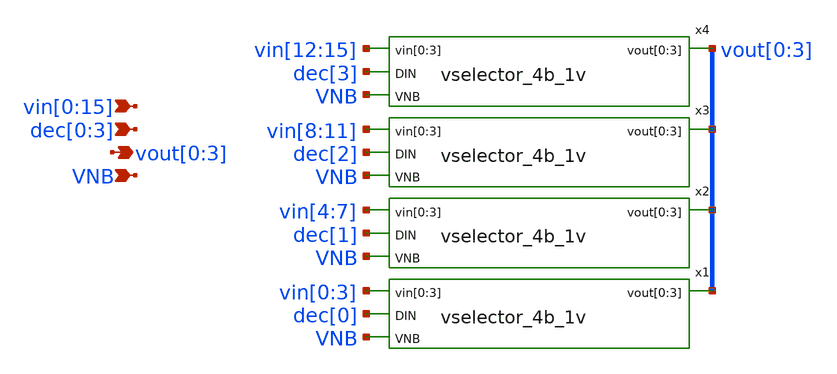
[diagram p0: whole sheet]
** sch_path: xschem/vselector_6b_1v_stage_2.sch
**.subckt vselector_6b_1v_stage_2
*+ vin[0],vin[1],vin[2],vin[3],vin[4],vin[5],vin[6],vin[7],vin[8],vin[9],vin[10],vin[11],vin[12],vin[13],vin[14],vin[15] vout[0],vout[1],vout[2],vout[3] VNB dec[0],dec[1],dec[2],dec[3]
*.ipin
*+ vin[0],vin[1],vin[2],vin[3],vin[4],vin[5],vin[6],vin[7],vin[8],vin[9],vin[10],vin[11],vin[12],vin[13],vin[14],vin[15]
*.opin vout[0],vout[1],vout[2],vout[3]
*.ipin VNB
*.ipin dec[0],dec[1],dec[2],dec[3]
x1 vin[0] vin[1] vin[2] vin[3] dec[0] vout[0] vout[1] vout[2] vout[3] VNB vselector_4b_1v
x2 vin[4] vin[5] vin[6] vin[7] dec[1] vout[0] vout[1] vout[2] vout[3] VNB vselector_4b_1v
x3 vin[8] vin[9] vin[10] vin[11] dec[2] vout[0] vout[1] vout[2] vout[3] VNB vselector_4b_1v
x4 vin[12] vin[13] vin[14] vin[15] dec[3] vout[0] vout[1] vout[2] vout[3] VNB vselector_4b_1v
**.ends

* expanding   symbol:  vselector_4b_1v.sym # of pins=4
** sym_path: xschem/vselector_4b_1v.sym
** sch_path: xschem/vselector_4b_1v.sch
.subckt vselector_4b_1v vin[0] vin[1] vin[2] vin[3] DIN vout[0] vout[1] vout[2] vout[3] VNB
*.ipin vin[0],vin[1],vin[2],vin[3]
*.opin vout[0],vout[1],vout[2],vout[3]
*.ipin VNB
*.ipin DIN
.param wp=0.42 wn=0.42 l=0.5

XM1 vout[0] DIN vin[0] VNB sky130_fd_pr__nfet_g5v0d10v5 L=l W=wn nf=1 ad='int((nf+1)/2) * W/nf * 0.29'
+ as='int((nf+2)/2) * W/nf * 0.29' pd='2*int((nf+1)/2) * (W/nf + 0.29)' ps='2*int((nf+2)/2) * (W/nf + 0.29)'
+ nrd='0.29 / W' nrs='0.29 / W' sa=0 sb=0 sd=0 mult=1 m=1
XM2 vout[1] DIN vin[1] VNB sky130_fd_pr__nfet_g5v0d10v5 L=l W=wn nf=1 ad='int((nf+1)/2) * W/nf * 0.29'
+ as='int((nf+2)/2) * W/nf * 0.29' pd='2*int((nf+1)/2) * (W/nf + 0.29)' ps='2*int((nf+2)/2) * (W/nf + 0.29)'
+ nrd='0.29 / W' nrs='0.29 / W' sa=0 sb=0 sd=0 mult=1 m=1
XM3 vout[2] DIN vin[2] VNB sky130_fd_pr__nfet_g5v0d10v5 L=l W=wn nf=1 ad='int((nf+1)/2) * W/nf * 0.29'
+ as='int((nf+2)/2) * W/nf * 0.29' pd='2*int((nf+1)/2) * (W/nf + 0.29)' ps='2*int((nf+2)/2) * (W/nf + 0.29)'
+ nrd='0.29 / W' nrs='0.29 / W' sa=0 sb=0 sd=0 mult=1 m=1
XM4 vout[3] DIN vin[3] VNB sky130_fd_pr__nfet_g5v0d10v5 L=l W=wn nf=1 ad='int((nf+1)/2) * W/nf * 0.29'
+ as='int((nf+2)/2) * W/nf * 0.29' pd='2*int((nf+1)/2) * (W/nf + 0.29)' ps='2*int((nf+2)/2) * (W/nf + 0.29)'
+ nrd='0.29 / W' nrs='0.29 / W' sa=0 sb=0 sd=0 mult=1 m=1
.ends

.end
